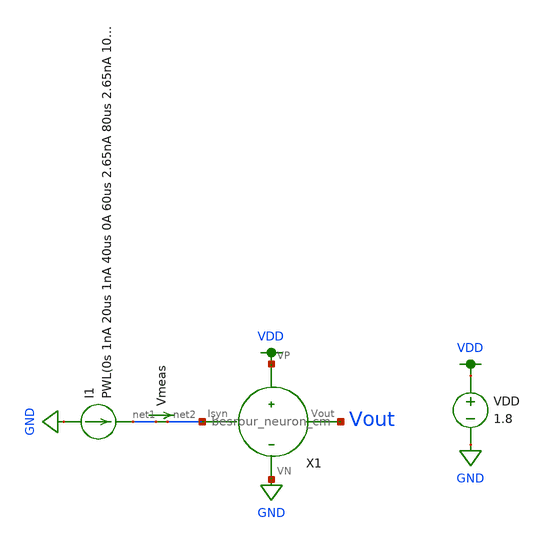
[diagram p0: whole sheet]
** sch_path: schematic/freq_besrour.sch
**.subckt freq_besrour
I1 GND net1 PWL(0s 1nA 20us 1nA 40us 0A 60us 2.65nA 80us 2.65nA 100us 0A 120us 7.02nA 140us 7.02nA
+ 160us 0A 180us 18.63nA 200us 18.63nA 220us 0A 240us 49.44nA 260us 49.44nA 280us 0A 300us 131.25nA 320us
+ 131.25nA 340us 0A 360us 348.22nA 380us 348.22nA 400us 0A 420us 924.21nA 440us 924.21nA 460us 0A 480us 2.45uA
+ 500us 2.45uA 520us 0A 540us 6.51uA 560us 6.51uA 580us 0A 600us 17.28uA 620us 17.28uA 640us 0A 660us
+ 45.86uA 680us 45.86uA 700us 0A 720us 121.67uA 740us 121.67uA 760us 0A 780us 323uA 800us 323uA 820us 0A
+ 840us 857uA 860us 857uA 880us 0A 900us 1mA 920us 1mA 940us 0A)

VDD VDD GND 1.8
X1 net2 Vout VDD GND besrour_neuron_cm
Vmeas net1 net2 0
.save i(vmeas)
**** begin user architecture code

.param W=2
.param L=0.3
.control
set wr_vecnames
set wr_singlescale
save all
tran 0.1n 640us
wrdata ~/neuromorphic_computing_final/simulation/test.txt i(vmeas) v(Vout)
set appendwrite
.endc



.option wnflag=1
.param MC_SWITCH=0.0
.lib ~/skywater/skywater-pdk/libraries/sky130_fd_pr_ngspice/latest/models/sky130.lib.spice tt

**** end user architecture code
**.ends

* expanding   symbol:  /home/madvlsi/neuromorphic_computing_final/schematic/besrour_neuron_cm.sym #
*+ of pins=4
** sym_path: schematic/besrour_neuron_cm.sym
** sch_path: schematic/besrour_neuron_cm.sch
.subckt besrour_neuron_cm Isyn Vout VP VN
*.iopin VP
*.iopin VN
*.iopin Isyn
*.opin Vout
XM2 VMEMINT net1 VP VDD sky130_fd_pr__pfet_01v8 L={L} W={W} nf=1 ad='int((nf+1)/2) * W/nf * 0.29' as='int((nf+2)/2) * W/nf * 0.29'
+ pd='2*int((nf+1)/2) * (W/nf + 0.29)' ps='2*int((nf+2)/2) * (W/nf + 0.29)' nrd='0.29 / W' nrs='0.29 / W'
+ sa=0 sb=0 sd=0 mult=1 m=1
XM3 VP net3 VMEMINT VDD sky130_fd_pr__pfet_01v8 L={L} W={W} nf=1 ad='int((nf+1)/2) * W/nf * 0.29' as='int((nf+2)/2) * W/nf * 0.29'
+ pd='2*int((nf+1)/2) * (W/nf + 0.29)' ps='2*int((nf+2)/2) * (W/nf + 0.29)' nrd='0.29 / W' nrs='0.29 / W'
+ sa=0 sb=0 sd=0 mult=1 m=1
XM4 net3 VMEMINT VP VDD sky130_fd_pr__pfet_01v8 L={L} W={W} nf=1 ad='int((nf+1)/2) * W/nf * 0.29' as='int((nf+2)/2) * W/nf * 0.29'
+ pd='2*int((nf+1)/2) * (W/nf + 0.29)' ps='2*int((nf+2)/2) * (W/nf + 0.29)' nrd='0.29 / W' nrs='0.29 / W'
+ sa=0 sb=0 sd=0 mult=1 m=1
XM5 net2 net3 VP VDD sky130_fd_pr__pfet_01v8 L={L} W={W} nf=1 ad='int((nf+1)/2) * W/nf * 0.29' as='int((nf+2)/2) * W/nf * 0.29'
+ pd='2*int((nf+1)/2) * (W/nf + 0.29)' ps='2*int((nf+2)/2) * (W/nf + 0.29)' nrd='0.29 / W' nrs='0.29 / W'
+ sa=0 sb=0 sd=0 mult=1 m=1
XM6 net3 VMEMINT VN GND sky130_fd_pr__nfet_01v8 L={L} W={W} nf=1 ad='int((nf+1)/2) * W/nf * 0.29' as='int((nf+2)/2) * W/nf * 0.29'
+ pd='2*int((nf+1)/2) * (W/nf + 0.29)' ps='2*int((nf+2)/2) * (W/nf + 0.29)' nrd='0.29 / W' nrs='0.29 / W'
+ sa=0 sb=0 sd=0 mult=1 m=1
XM8 net2 net3 VN GND sky130_fd_pr__nfet_01v8 L={L} W={W} nf=1 ad='int((nf+1)/2) * W/nf * 0.29' as='int((nf+2)/2) * W/nf * 0.29'
+ pd='2*int((nf+1)/2) * (W/nf + 0.29)' ps='2*int((nf+2)/2) * (W/nf + 0.29)' nrd='0.29 / W' nrs='0.29 / W'
+ sa=0 sb=0 sd=0 mult=1 m=1
C1 VMEMINT VN 340f m=1
C2 net2 VN 340f m=1
XM9 net4 net2 VP VDD sky130_fd_pr__pfet_01v8 L={L} W={W} nf=1 ad='int((nf+1)/2) * W/nf * 0.29' as='int((nf+2)/2) * W/nf * 0.29'
+ pd='2*int((nf+1)/2) * (W/nf + 0.29)' ps='2*int((nf+2)/2) * (W/nf + 0.29)' nrd='0.29 / W' nrs='0.29 / W'
+ sa=0 sb=0 sd=0 mult=1 m=1
XM10 net4 net2 VN GND sky130_fd_pr__nfet_01v8 L={L} W={W} nf=1 ad='int((nf+1)/2) * W/nf * 0.29' as='int((nf+2)/2) * W/nf * 0.29'
+ pd='2*int((nf+1)/2) * (W/nf + 0.29)' ps='2*int((nf+2)/2) * (W/nf + 0.29)' nrd='0.29 / W' nrs='0.29 / W'
+ sa=0 sb=0 sd=0 mult=1 m=1
XM11 Vout net4 VP VDD sky130_fd_pr__pfet_01v8 L={L} W={W} nf=1 ad='int((nf+1)/2) * W/nf * 0.29' as='int((nf+2)/2) * W/nf * 0.29'
+ pd='2*int((nf+1)/2) * (W/nf + 0.29)' ps='2*int((nf+2)/2) * (W/nf + 0.29)' nrd='0.29 / W' nrs='0.29 / W'
+ sa=0 sb=0 sd=0 mult=1 m=1
XM12 Vout net4 VN GND sky130_fd_pr__nfet_01v8 L={L} W={W} nf=1 ad='int((nf+1)/2) * W/nf * 0.29' as='int((nf+2)/2) * W/nf * 0.29'
+ pd='2*int((nf+1)/2) * (W/nf + 0.29)' ps='2*int((nf+2)/2) * (W/nf + 0.29)' nrd='0.29 / W' nrs='0.29 / W'
+ sa=0 sb=0 sd=0 mult=1 m=1
XM13 net1 Isyn VN GND sky130_fd_pr__nfet_01v8 L={L} W={W} nf=1 ad='int((nf+1)/2) * W/nf * 0.29' as='int((nf+2)/2) * W/nf * 0.29'
+ pd='2*int((nf+1)/2) * (W/nf + 0.29)' ps='2*int((nf+2)/2) * (W/nf + 0.29)' nrd='0.29 / W' nrs='0.29 / W'
+ sa=0 sb=0 sd=0 mult=1 m=1
XM14 VN Isyn Isyn GND sky130_fd_pr__nfet_01v8 L={L} W={W} nf=1 ad='int((nf+1)/2) * W/nf * 0.29' as='int((nf+2)/2) * W/nf * 0.29'
+ pd='2*int((nf+1)/2) * (W/nf + 0.29)' ps='2*int((nf+2)/2) * (W/nf + 0.29)' nrd='0.29 / W' nrs='0.29 / W'
+ sa=0 sb=0 sd=0 mult=1 m=1
XM1 VP net1 net1 VDD sky130_fd_pr__pfet_01v8 L={L} W={W} nf=1 ad='int((nf+1)/2) * W/nf * 0.29' as='int((nf+2)/2) * W/nf * 0.29'
+ pd='2*int((nf+1)/2) * (W/nf + 0.29)' ps='2*int((nf+2)/2) * (W/nf + 0.29)' nrd='0.29 / W' nrs='0.29 / W'
+ sa=0 sb=0 sd=0 mult=1 m=1
XM7 VN net2 VMEMINT GND sky130_fd_pr__nfet_01v8 L={L} W={W} nf=1 ad='int((nf+1)/2) * W/nf * 0.29' as='int((nf+2)/2) * W/nf * 0.29'
+ pd='2*int((nf+1)/2) * (W/nf + 0.29)' ps='2*int((nf+2)/2) * (W/nf + 0.29)' nrd='0.29 / W' nrs='0.29 / W'
+ sa=0 sb=0 sd=0 mult=1 m=1
.ends

.GLOBAL GND
.GLOBAL VDD
.end
